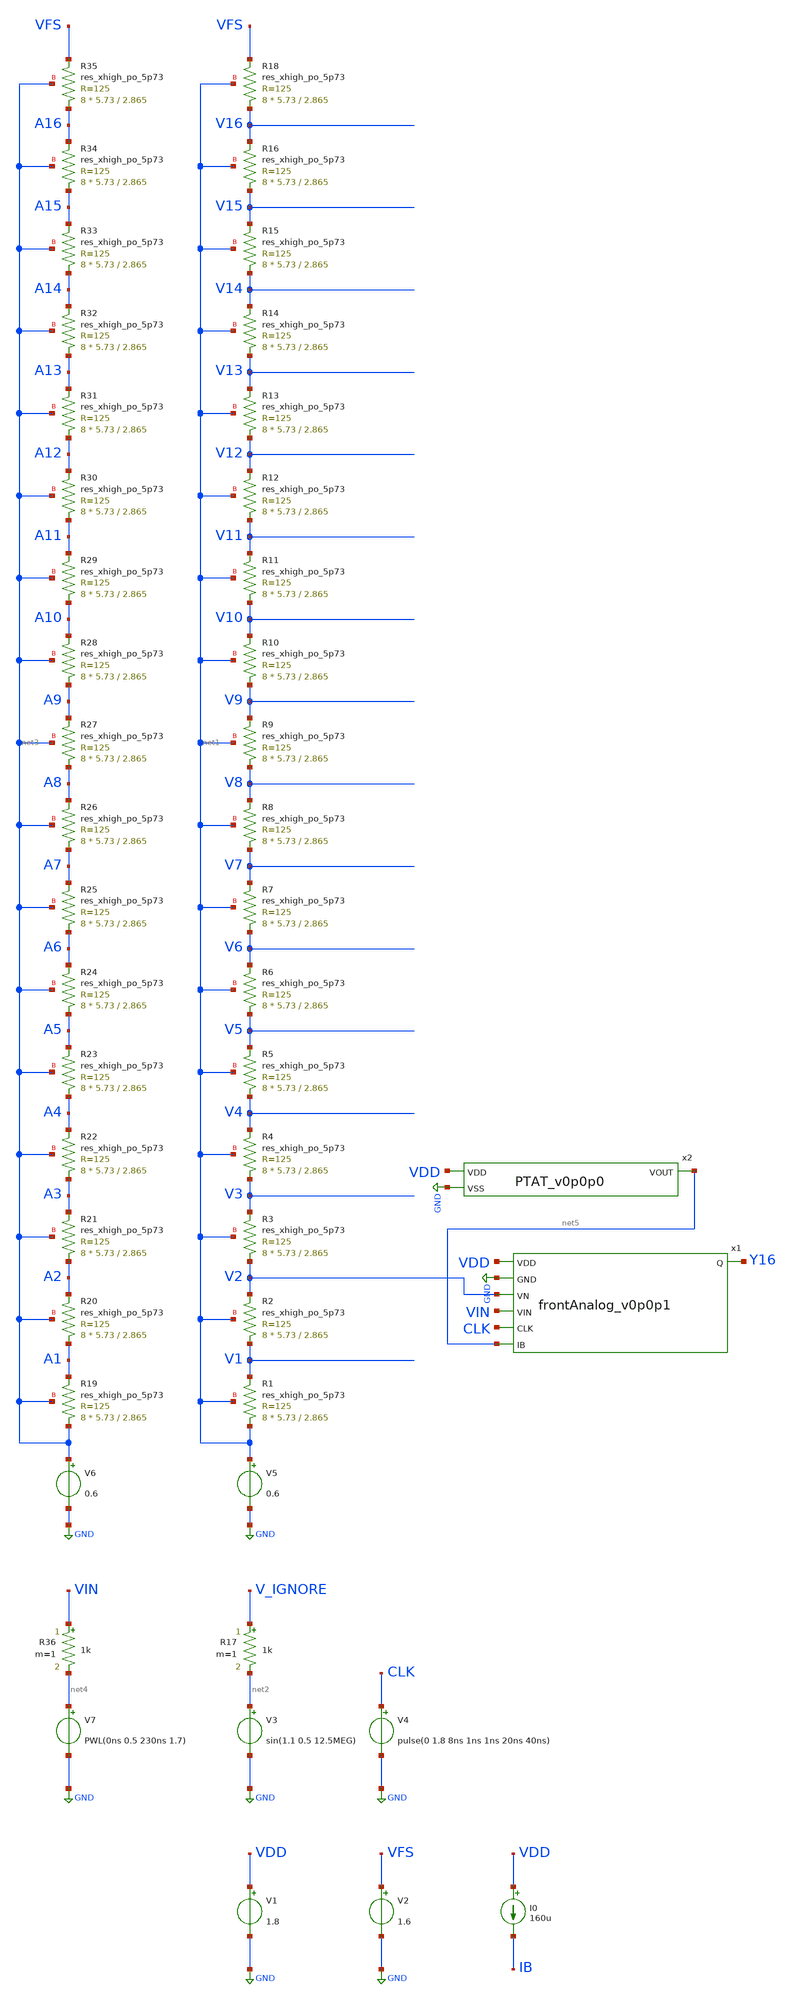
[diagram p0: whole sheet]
** sch_path: testbench/flash_ADC_4b_v2.sch
.lib $::SKYWATER_MODELS/sky130.lib.spice tt
.include $::SKYWATER_STDCELLS/sky130_fd_sc_hd.spice

**.subckt flash_ADC_4b_v2
V3 net2 GND sin(1.1 0.5 12.5MEG)
V4 CLK GND pulse(0 1.8 8ns 1ns 1ns 20ns 40ns)
V1 VDD GND 1.8
V2 VFS GND 1.6
R17 V_IGNORE net2 1k m=1
I0 VDD IB 160u
V5 net1 GND 0.6
XR19 net3 A1 net3 sky130_fd_pr__res_xhigh_po_5p73 L=2.865 mult=8 m=8
V6 net3 GND 0.6
XR20 A1 A2 net3 sky130_fd_pr__res_xhigh_po_5p73 L=2.865 mult=8 m=8
XR21 A2 A3 net3 sky130_fd_pr__res_xhigh_po_5p73 L=2.865 mult=8 m=8
XR22 A3 A4 net3 sky130_fd_pr__res_xhigh_po_5p73 L=2.865 mult=8 m=8
XR23 A4 A5 net3 sky130_fd_pr__res_xhigh_po_5p73 L=2.865 mult=8 m=8
XR24 A5 A6 net3 sky130_fd_pr__res_xhigh_po_5p73 L=2.865 mult=8 m=8
XR25 A6 A7 net3 sky130_fd_pr__res_xhigh_po_5p73 L=2.865 mult=8 m=8
XR26 A7 A8 net3 sky130_fd_pr__res_xhigh_po_5p73 L=2.865 mult=8 m=8
XR27 A8 A9 net3 sky130_fd_pr__res_xhigh_po_5p73 L=2.865 mult=8 m=8
XR28 A9 A10 net3 sky130_fd_pr__res_xhigh_po_5p73 L=2.865 mult=8 m=8
XR29 A10 A11 net3 sky130_fd_pr__res_xhigh_po_5p73 L=2.865 mult=8 m=8
XR30 A11 A12 net3 sky130_fd_pr__res_xhigh_po_5p73 L=2.865 mult=8 m=8
XR31 A12 A13 net3 sky130_fd_pr__res_xhigh_po_5p73 L=2.865 mult=8 m=8
XR32 A13 A14 net3 sky130_fd_pr__res_xhigh_po_5p73 L=2.865 mult=8 m=8
XR33 A14 A15 net3 sky130_fd_pr__res_xhigh_po_5p73 L=2.865 mult=8 m=8
XR34 A15 A16 net3 sky130_fd_pr__res_xhigh_po_5p73 L=2.865 mult=8 m=8
XR35 A16 VFS net3 sky130_fd_pr__res_xhigh_po_5p73 L=2.865 mult=8 m=8
XR1 net1 V1 net1 sky130_fd_pr__res_xhigh_po_5p73 L=2.865 mult=8 m=8
XR2 V1 V2 net1 sky130_fd_pr__res_xhigh_po_5p73 L=2.865 mult=8 m=8
XR3 V2 V3 net1 sky130_fd_pr__res_xhigh_po_5p73 L=2.865 mult=8 m=8
XR4 V3 V4 net1 sky130_fd_pr__res_xhigh_po_5p73 L=2.865 mult=8 m=8
XR5 V4 V5 net1 sky130_fd_pr__res_xhigh_po_5p73 L=2.865 mult=8 m=8
XR6 V5 V6 net1 sky130_fd_pr__res_xhigh_po_5p73 L=2.865 mult=8 m=8
XR7 V6 V7 net1 sky130_fd_pr__res_xhigh_po_5p73 L=2.865 mult=8 m=8
XR8 V7 V8 net1 sky130_fd_pr__res_xhigh_po_5p73 L=2.865 mult=8 m=8
XR9 V8 V9 net1 sky130_fd_pr__res_xhigh_po_5p73 L=2.865 mult=8 m=8
XR10 V9 V10 net1 sky130_fd_pr__res_xhigh_po_5p73 L=2.865 mult=8 m=8
XR11 V10 V11 net1 sky130_fd_pr__res_xhigh_po_5p73 L=2.865 mult=8 m=8
XR12 V11 V12 net1 sky130_fd_pr__res_xhigh_po_5p73 L=2.865 mult=8 m=8
XR13 V12 V13 net1 sky130_fd_pr__res_xhigh_po_5p73 L=2.865 mult=8 m=8
XR14 V13 V14 net1 sky130_fd_pr__res_xhigh_po_5p73 L=2.865 mult=8 m=8
XR15 V14 V15 net1 sky130_fd_pr__res_xhigh_po_5p73 L=2.865 mult=8 m=8
XR16 V15 V16 net1 sky130_fd_pr__res_xhigh_po_5p73 L=2.865 mult=8 m=8
XR18 V16 VFS net1 sky130_fd_pr__res_xhigh_po_5p73 L=2.865 mult=8 m=8
V7 net4 GND PWL(0ns 0.5 230ns 1.7)
R36 VIN net4 1k m=1
x1 VDD GND V2 VIN CLK Y16 net5 frontAnalog_v0p0p1
x2 VDD net5 GND PTAT_v0p0p0
**** begin user architecture code


.options savecurrents
.control

save all

tran 0.005n 240n
remzerovec
write flash_ADC_4b_v2.raw

.endc


**** end user architecture code
**.ends
.GLOBAL GND
.end
